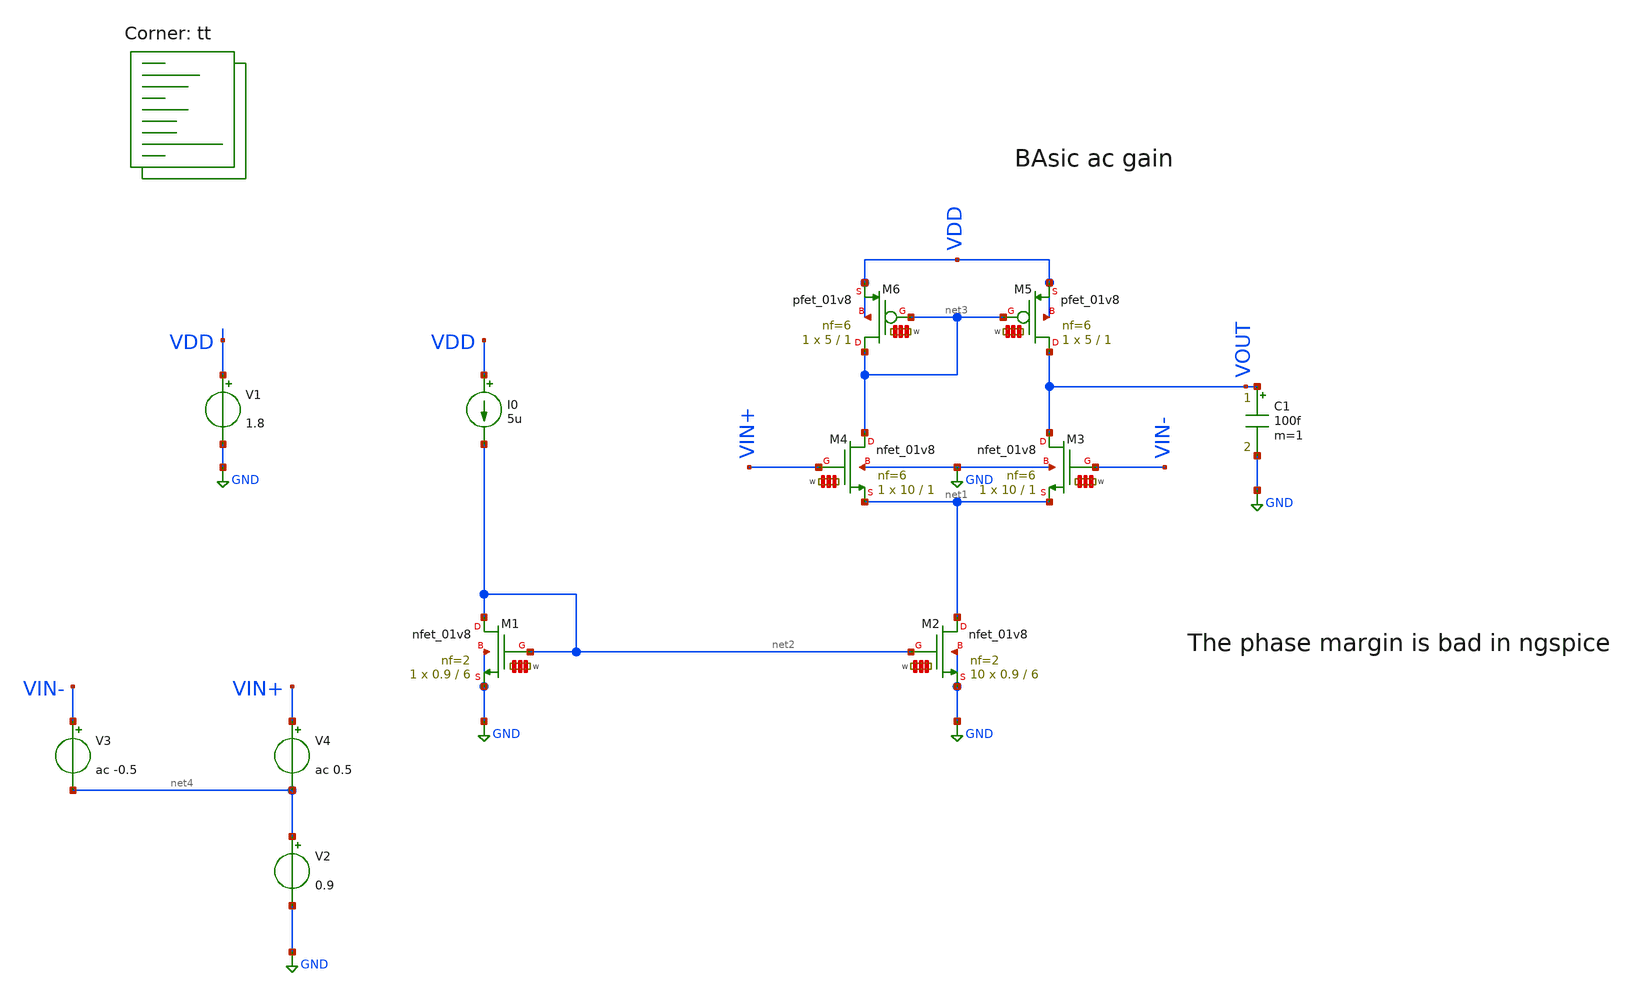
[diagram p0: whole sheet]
** sch_path: amplifiers/basic/NMOS_diff_pair_1stage/NMOS.sch
**.subckt NMOS
V1 VDD GND 1.8
I0 VDD net2 5u
XM2 net1 net2 GND GND sky130_fd_pr__nfet_01v8 L=6 W='0.9 * 2 ' nf=2 ad='int((2 + 1)/2) * 0.9 / 2 * 0.29'
+ as='int((2 + 2)/2) * 0.9 / 2 * 0.29' pd='2*int((2 + 1)/2) * (0.9 / 2 + 0.29)' ps='2*int((2 + 2)/2) * (0.9 / 2 + 0.29)'
+ nrd='0.29 / 0.9 ' nrs='0.29 / 0.9 ' sa=0 sb=0 sd=0 mult=10 m=10
XM1 net2 net2 GND GND sky130_fd_pr__nfet_01v8 L=6 W='0.9 * 2 ' nf=2 ad='int((2 + 1)/2) * 0.9 / 2 * 0.29'
+ as='int((2 + 2)/2) * 0.9 / 2 * 0.29' pd='2*int((2 + 1)/2) * (0.9 / 2 + 0.29)' ps='2*int((2 + 2)/2) * (0.9 / 2 + 0.29)'
+ nrd='0.29 / 0.9 ' nrs='0.29 / 0.9 ' sa=0 sb=0 sd=0 mult=1 m=1
XM3 VOUT VIN- net1 GND sky130_fd_pr__nfet_01v8 L=1 W='10 * 6 ' nf=6 ad='int((6 + 1)/2) * 10 / 6 * 0.29'
+ as='int((6 + 2)/2) * 10 / 6 * 0.29' pd='2*int((6 + 1)/2) * (10 / 6 + 0.29)' ps='2*int((6 + 2)/2) * (10 / 6 + 0.29)'
+ nrd='0.29 / 10 ' nrs='0.29 / 10 ' sa=0 sb=0 sd=0 mult=1 m=1
XM6 net3 net3 VDD VDD sky130_fd_pr__pfet_01v8 L=1 W='5 * 6 ' nf=6 ad= as='int((6 + 2)/2) * 5 * 0.29'
+ pd='2*int((6 + 1)/2) * (5 + 0.29)' ps='2*int((6 + 2)/2) * (5 + 0.29)' nrd='0.29 / 5 / 6 ' nrs='0.29 / 5 / 6 '
+ sa=0 sb=0 sd=0 mult=1 m=1
C1 VOUT GND 100f m=1
XM4 net3 VIN+ net1 GND sky130_fd_pr__nfet_01v8 L=1 W='10 * 6 ' nf=6 ad='int((6 + 1)/2) * 10 / 6 * 0.29'
+ as='int((6 + 2)/2) * 10 / 6 * 0.29' pd='2*int((6 + 1)/2) * (10 / 6 + 0.29)' ps='2*int((6 + 2)/2) * (10 / 6 + 0.29)'
+ nrd='0.29 / 10 ' nrs='0.29 / 10 ' sa=0 sb=0 sd=0 mult=1 m=1
XM5 VOUT net3 VDD VDD sky130_fd_pr__pfet_01v8 L=1 W='5 * 6 ' nf=6 ad= as='int((6 + 2)/2) * 5 * 0.29'
+ pd='2*int((6 + 1)/2) * (5 + 0.29)' ps='2*int((6 + 2)/2) * (5 + 0.29)' nrd='0.29 / 5 / 6 ' nrs='0.29 / 5 / 6 '
+ sa=0 sb=0 sd=0 mult=1 m=1
V2 net4 GND 0.9
V4 VIN+ net4 ac 0.5
V3 VIN- net4 ac -0.5
**** begin user architecture code
.lib $::SKYWATER_MODELS/sky130.lib.spice tt

**************************************************************
**************************************************************
**************************************************************
**************************************************************
**************************************************************
*LIBs*********************************************************
**************************************************************
**************************************************************
**************************************************************
**************************************************************
**************************************************************
*.lib $::SKYWATER_MODELS/sky130.lib.spice tt
* chose the corners in the corner file
* tt_mm for mismatch
* ss ff sf fs standart corners
* ll hh lh hl capacitor and resistors corners
* mc for total process variation including corners
**************************************************************
**************************************************************
**************************************************************
**************************************************************
**************************************************************
*Corners/montecarlo options***********************************
**************************************************************
**************************************************************
**************************************************************
**************************************************************
**************************************************************
.TEMP 27
**************************************************************
**************************************************************
**************************************************************
**************************************************************
*SIMULATION and Plots*****************************************
**************************************************************
**************************************************************
**************************************************************
**************************************************************
.control
save all
ac dec 20 1 50G
plot db(v(VOUT))
plot ph(v(VOUT))
.endc

**** end user architecture code
**.ends
.GLOBAL GND
.end
